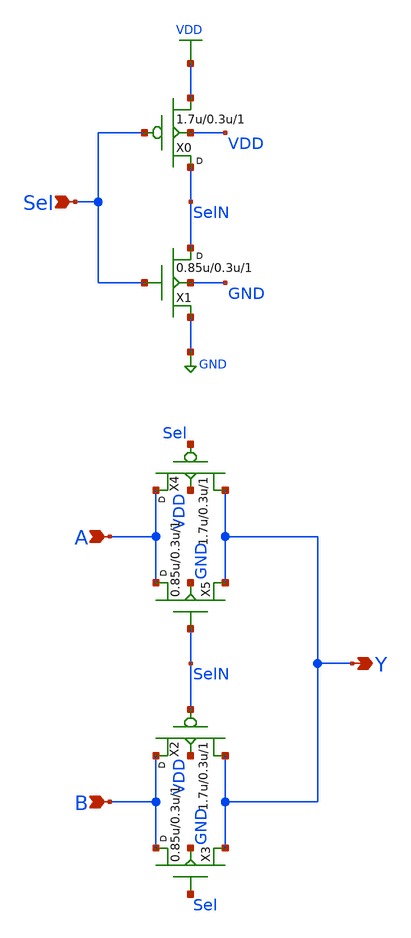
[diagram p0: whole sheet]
** sch_path: lib/xschem/gf180mcu_osu_sc_12T_mux2_1.sch
**.subckt gf180mcu_osu_sc_12T_mux2_1 Sel A B Y
*.ipin Sel
*.ipin A
*.ipin B
*.opin Y
X0 SelN Sel VDD VDD pmos_3p3 w=1.7u l=0.3u m=1
X1 SelN Sel GND GND nmos_3p3 w=0.85u l=0.3u m=1
X2 B SelN Y VDD pmos_3p3 w=1.7u l=0.3u m=1
X3 B Sel Y GND nmos_3p3 w=0.85u l=0.3u m=1
X4 A Sel Y VDD pmos_3p3 w=1.7u l=0.3u m=1
X5 A SelN Y GND nmos_3p3 w=0.85u l=0.3u m=1
**** begin user architecture code


.inc "/import/yukari1/lrburle/OSU_180/char/techfiles/design.hspice"
.lib "/import/yukari1/lrburle/OSU_180/char/techfiles/sm141064.hspice" typical


**** end user architecture code
**.ends
.GLOBAL VDD
.GLOBAL GND
.end
